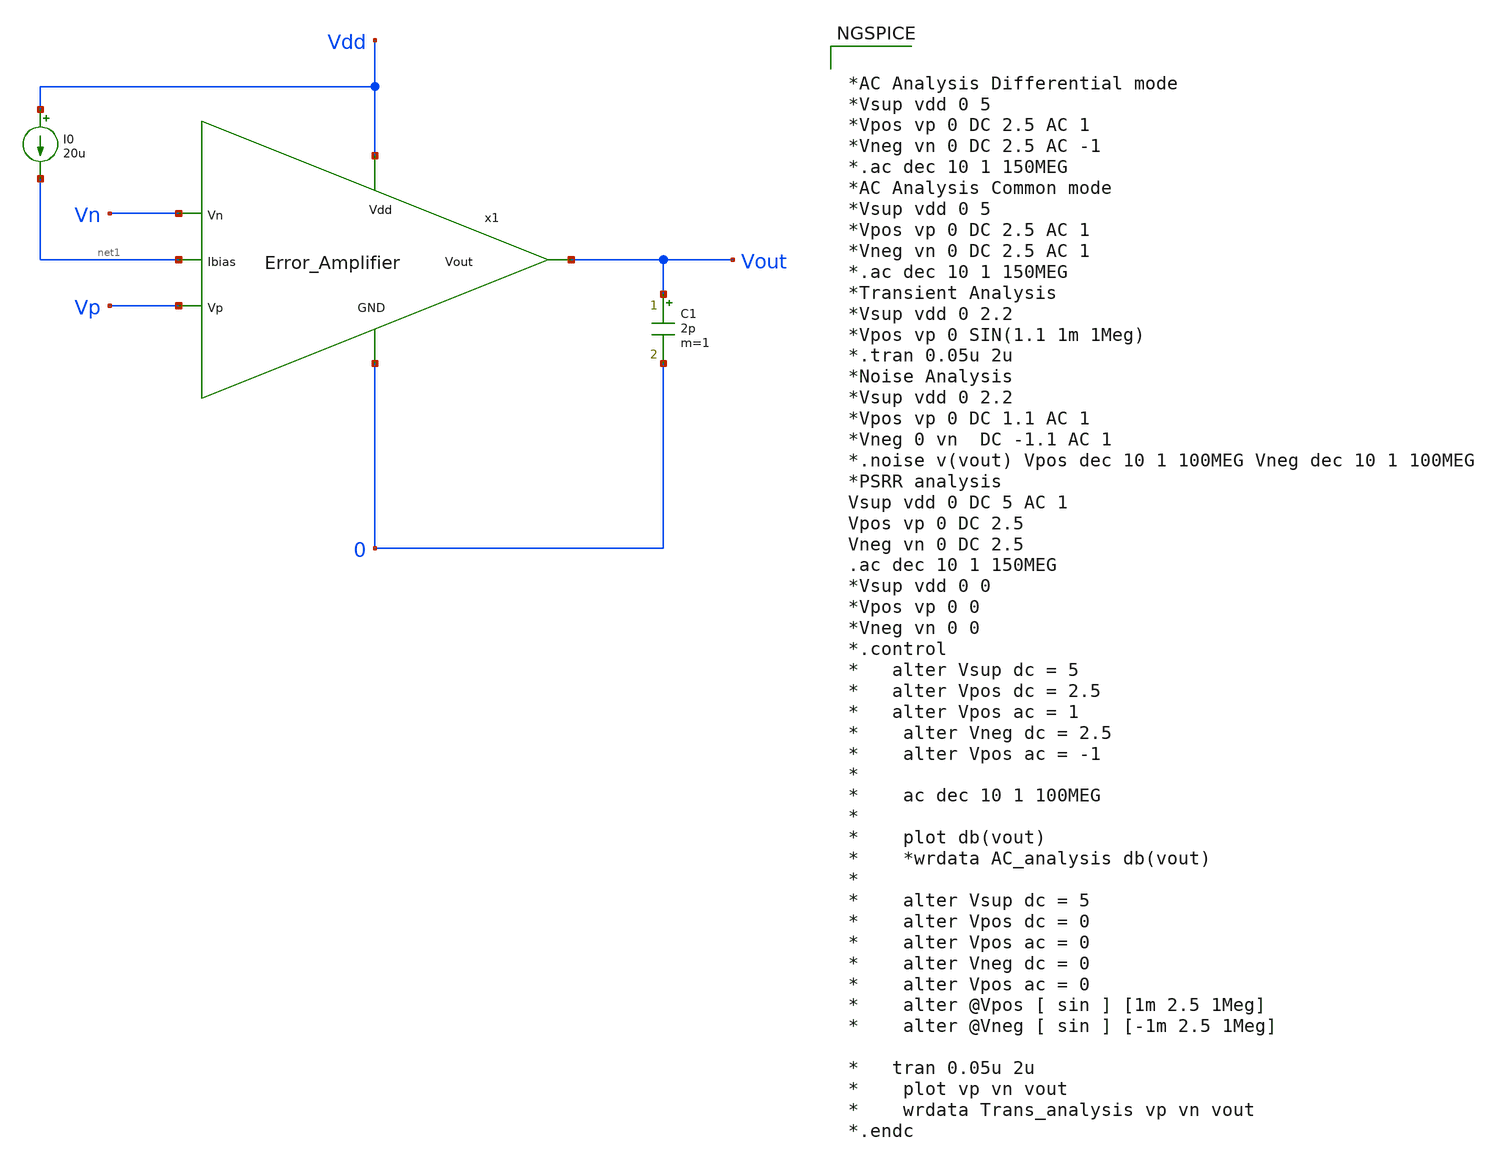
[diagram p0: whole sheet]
** sch_path: Analog_Blocks/LDO/Schematic/Error_Amplifier_TB.sch
**.subckt Error_Amplifier_TB
x1 Vdd Vn Vp Vout net1 0 Error_Amplifier
C1 Vout 0 2p m=1
I0 Vdd net1 20u
**** begin user architecture code


*AC Analysis Differential mode
*Vsup vdd 0 5
*Vpos vp 0 DC 2.5 AC 1
*Vneg vn 0 DC 2.5 AC -1
*.ac dec 10 1 150MEG
*AC Analysis Common mode
*Vsup vdd 0 5
*Vpos vp 0 DC 2.5 AC 1
*Vneg vn 0 DC 2.5 AC 1
*.ac dec 10 1 150MEG
*Transient Analysis
*Vsup vdd 0 2.2
*Vpos vp 0 SIN(1.1 1m 1Meg)
*.tran 0.05u 2u
*Noise Analysis
*Vsup vdd 0 2.2
*Vpos vp 0 DC 1.1 AC 1
*Vneg 0 vn  DC -1.1 AC 1
*.noise v(vout) Vpos dec 10 1 100MEG Vneg dec 10 1 100MEG
*PSRR analysis
Vsup vdd 0 DC 5 AC 1
Vpos vp 0 DC 2.5
Vneg vn 0 DC 2.5
.ac dec 10 1 150MEG
*Vsup vdd 0 0
*Vpos vp 0 0
*Vneg vn 0 0
*.control
*   alter Vsup dc = 5
*   alter Vpos dc = 2.5
*   alter Vpos ac = 1
*    alter Vneg dc = 2.5
*    alter Vpos ac = -1
*
*    ac dec 10 1 100MEG
*
*    plot db(vout)
*    *wrdata AC_analysis db(vout)
*
*    alter Vsup dc = 5
*    alter Vpos dc = 0
*    alter Vpos ac = 0
*    alter Vneg dc = 0
*    alter Vpos ac = 0
*    alter @Vpos [ sin ] [1m 2.5 1Meg]
*    alter @Vneg [ sin ] [-1m 2.5 1Meg]

*   tran 0.05u 2u
*    plot vp vn vout
*    wrdata Trans_analysis vp vn vout
*.endc




.include $::SKYWATER_MODELS/cells/nfet_01v8/sky130_fd_pr__nfet_01v8__tt.corner.spice
.include $::SKYWATER_MODELS/cells/nfet_01v8_lvt/sky130_fd_pr__nfet_01v8_lvt__tt.corner.spice
.include $::SKYWATER_MODELS/cells/pfet_01v8/sky130_fd_pr__pfet_01v8__tt.corner.spice
.include $::SKYWATER_MODELS/cells/nfet_03v3_nvt/sky130_fd_pr__nfet_03v3_nvt__tt.corner.spice
.include $::SKYWATER_MODELS/cells/nfet_05v0_nvt/sky130_fd_pr__nfet_05v0_nvt__tt.corner.spice
.include $::SKYWATER_MODELS/cells/esd_nfet_01v8/sky130_fd_pr__esd_nfet_01v8__tt.corner.spice
.include $::SKYWATER_MODELS/cells/pfet_01v8_lvt/sky130_fd_pr__pfet_01v8_lvt__tt.corner.spice
.include $::SKYWATER_MODELS/cells/pfet_01v8_hvt/sky130_fd_pr__pfet_01v8_hvt__tt.corner.spice
.include $::SKYWATER_MODELS/cells/esd_pfet_g5v0d10v5/sky130_fd_pr__esd_pfet_g5v0d10v5__tt.corner.spice
.include $::SKYWATER_MODELS/cells/pfet_g5v0d10v5/sky130_fd_pr__pfet_g5v0d10v5__tt.corner.spice
.include $::SKYWATER_MODELS/cells/pfet_g5v0d16v0/sky130_fd_pr__pfet_g5v0d16v0__tt.corner.spice
.include $::SKYWATER_MODELS/cells/nfet_g5v0d10v5/sky130_fd_pr__nfet_g5v0d10v5__tt.corner.spice
.include $::SKYWATER_MODELS/cells/nfet_g5v0d16v0/sky130_fd_pr__nfet_g5v0d16v0__tt_discrete.corner.spice
.include $::SKYWATER_MODELS/cells/esd_nfet_g5v0d10v5/sky130_fd_pr__esd_nfet_g5v0d10v5__tt.corner.spice
.include $::SKYWATER_MODELS/models/corners/tt/nonfet.spice
* Mismatch parameters
.include $::SKYWATER_MODELS/cells/nfet_01v8/sky130_fd_pr__nfet_01v8__mismatch.corner.spice
.include $::SKYWATER_MODELS/cells/pfet_01v8/sky130_fd_pr__pfet_01v8__mismatch.corner.spice
.include $::SKYWATER_MODELS/cells/nfet_01v8_lvt/sky130_fd_pr__nfet_01v8_lvt__mismatch.corner.spice
.include $::SKYWATER_MODELS/cells/pfet_01v8_lvt/sky130_fd_pr__pfet_01v8_lvt__mismatch.corner.spice
.include $::SKYWATER_MODELS/cells/pfet_01v8_hvt/sky130_fd_pr__pfet_01v8_hvt__mismatch.corner.spice
.include $::SKYWATER_MODELS/cells/nfet_g5v0d10v5/sky130_fd_pr__nfet_g5v0d10v5__mismatch.corner.spice
.include $::SKYWATER_MODELS/cells/pfet_g5v0d10v5/sky130_fd_pr__pfet_g5v0d10v5__mismatch.corner.spice
.include $::SKYWATER_MODELS/cells/nfet_05v0_nvt/sky130_fd_pr__nfet_05v0_nvt__mismatch.corner.spice
.include $::SKYWATER_MODELS/cells/nfet_03v3_nvt/sky130_fd_pr__nfet_03v3_nvt__mismatch.corner.spice
* Resistor$::SKYWATER_MODELS/Capacitor
.include $::SKYWATER_MODELS/models/r+c/res_typical__cap_typical.spice
.include $::SKYWATER_MODELS/models/r+c/res_typical__cap_typical__lin.spice
* Special cells
.include $::SKYWATER_MODELS/models/corners/tt/specialized_cells.spice
* All models
.include $::SKYWATER_MODELS/models/all.spice
* Corner
.include $::SKYWATER_MODELS/models/corners/tt/rf.spice

**** end user architecture code
**.ends
.end
